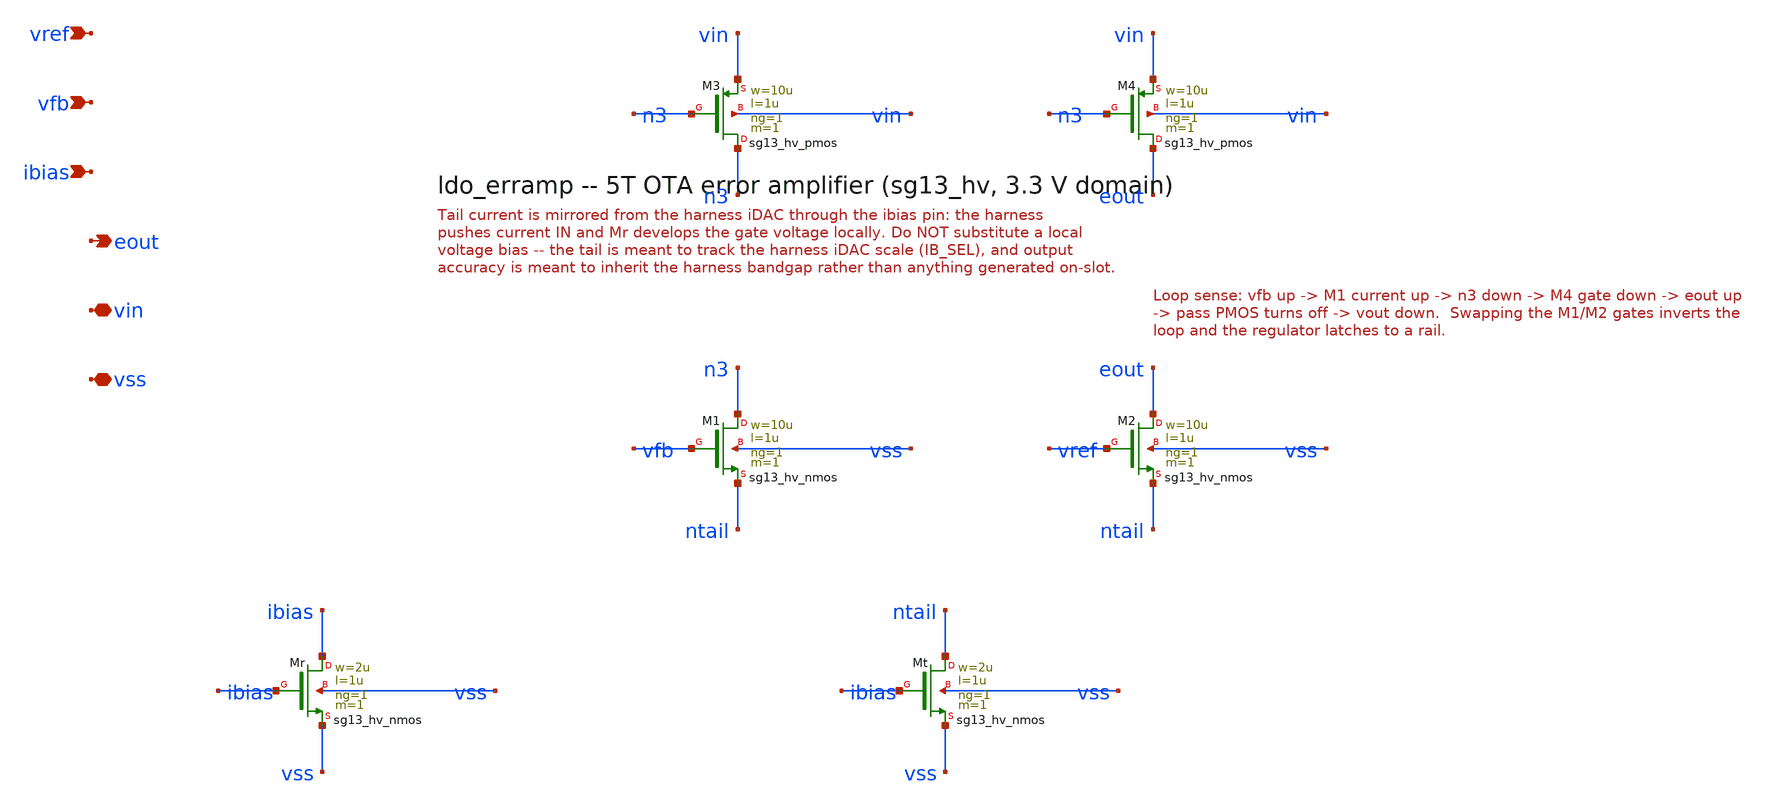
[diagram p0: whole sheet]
** sch_path: xschem/ldo_erramp.sch
**.subckt ldo_erramp vref vfb ibias eout vin vss
*.ipin vref
*.ipin vfb
*.ipin ibias
*.opin eout
*.iopin vin
*.iopin vss
XM3 n3 n3 vin vin sg13_hv_pmos w=10u l=1u ng=1 m=1 mm_ok=1
XM4 eout n3 vin vin sg13_hv_pmos w=10u l=1u ng=1 m=1 mm_ok=1
XM1 n3 vfb ntail vss sg13_hv_nmos w=10u l=1u ng=1 m=1 mm_ok=1
XM2 eout vref ntail vss sg13_hv_nmos w=10u l=1u ng=1 m=1 mm_ok=1
XMt ntail ibias vss vss sg13_hv_nmos w=2u l=1u ng=1 m=1 mm_ok=1
XMr ibias ibias vss vss sg13_hv_nmos w=2u l=1u ng=1 m=1 mm_ok=1
**.ends
.end
